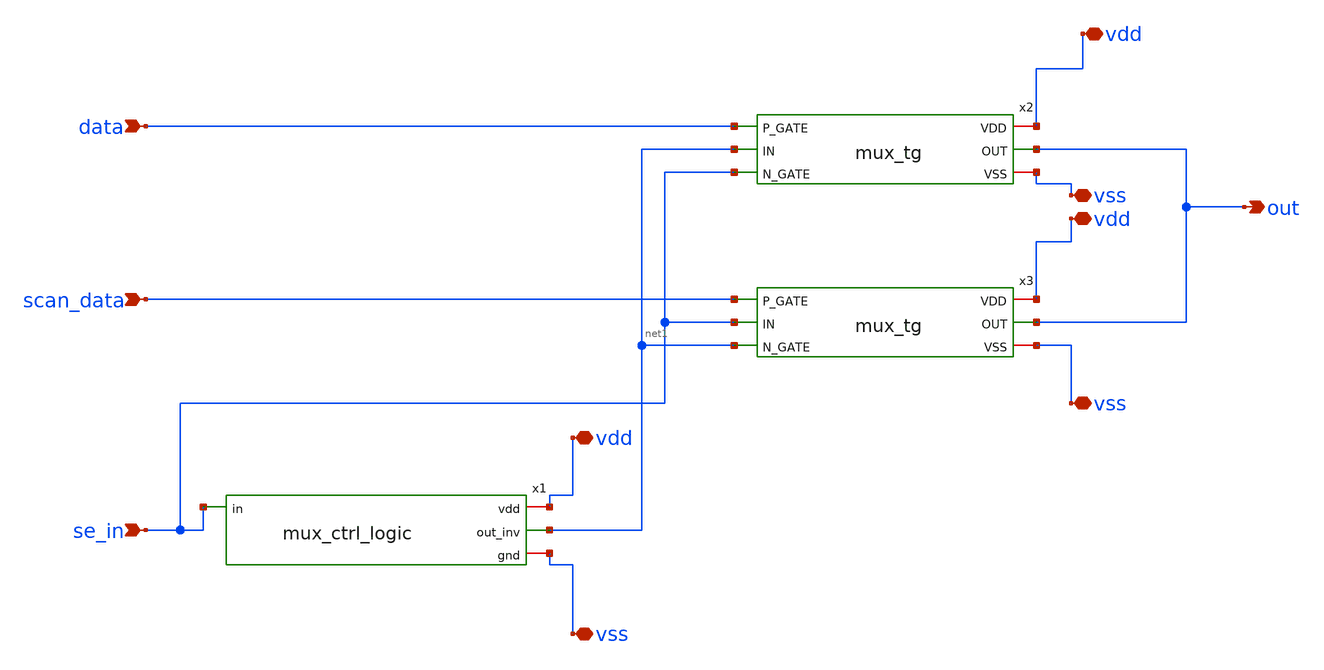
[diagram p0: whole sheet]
** sch_path: designs/schematics/mux2x1_transmission_gate/mux_toplevel.sch
**.subckt mux_toplevel vdd out data scan_data se_in vdd vss vss vdd vss
*.iopin vdd
*.opin out
*.ipin data
*.ipin scan_data
*.ipin se_in
*.iopin vdd
*.iopin vss
*.iopin vss
*.iopin vdd
*.iopin vss
x2 vdd data net1 out se_in vss mux_tg
x3 vdd scan_data se_in out net1 vss mux_tg
x1 vdd se_in net1 vss mux_ctrl_logic
**.ends

* expanding   symbol:  schematics/mux2x1_transmission_gate/mux_tg.sym # of pins=6
** sym_path: designs/cells/sdffrq/sch/mux_tg.sym
** sch_path: designs/cells/sdffrq/sch/mux_tg.sch
.subckt mux_tg VDD P_GATE IN OUT N_GATE VSS
*.iopin VDD
*.iopin VSS
*.opin OUT
*.ipin IN
*.ipin P_GATE
*.ipin N_GATE
XM1 IN N_GATE OUT VSS nfet_03v3 L=0.3u W=0.85u nf=1 ad='int((nf+1)/2) * W/nf * 0.18u' as='int((nf+2)/2) * W/nf * 0.18u'
+ pd='2*int((nf+1)/2) * (W/nf + 0.18u)' ps='2*int((nf+2)/2) * (W/nf + 0.18u)' nrd='0.18u / W' nrs='0.18u / W'
+ sa=0 sb=0 sd=0 m=1
XM2 IN P_GATE OUT VDD pfet_03v3 L=0.3u W=1.7u nf=1 ad='int((nf+1)/2) * W/nf * 0.18u' as='int((nf+2)/2) * W/nf * 0.18u'
+ pd='2*int((nf+1)/2) * (W/nf + 0.18u)' ps='2*int((nf+2)/2) * (W/nf + 0.18u)' nrd='0.18u / W' nrs='0.18u / W'
+ sa=0 sb=0 sd=0 m=1
.ends


* expanding   symbol:  schematics/mux2x1_transmission_gate/mux_ctrl_logic.sym # of pins=4
** sym_path: designs/schematics/mux2x1_transmission_gate/mux_ctrl_logic.sym
** sch_path: designs/schematics/mux2x1_transmission_gate/mux_ctrl_logic.sch
.subckt mux_ctrl_logic vdd in out_inv gnd
*.iopin vdd
*.iopin gnd
*.iopin out_inv
*.iopin in
XM1 out_inv in gnd gnd nfet_03v3 L=0.28u W=0.22u nf=1 ad='int((nf+1)/2) * W/nf * 0.18u' as='int((nf+2)/2) * W/nf * 0.18u'
+ pd='2*int((nf+1)/2) * (W/nf + 0.18u)' ps='2*int((nf+2)/2) * (W/nf + 0.18u)' nrd='0.18u / W' nrs='0.18u / W'
+ sa=0 sb=0 sd=0 m=1
XM2 out_inv in vdd vdd pfet_03v3 L=0.28u W=0.22u nf=1 ad='int((nf+1)/2) * W/nf * 0.18u' as='int((nf+2)/2) * W/nf * 0.18u'
+ pd='2*int((nf+1)/2) * (W/nf + 0.18u)' ps='2*int((nf+2)/2) * (W/nf + 0.18u)' nrd='0.18u / W' nrs='0.18u / W'
+ sa=0 sb=0 sd=0 m=1
.ends

.end
